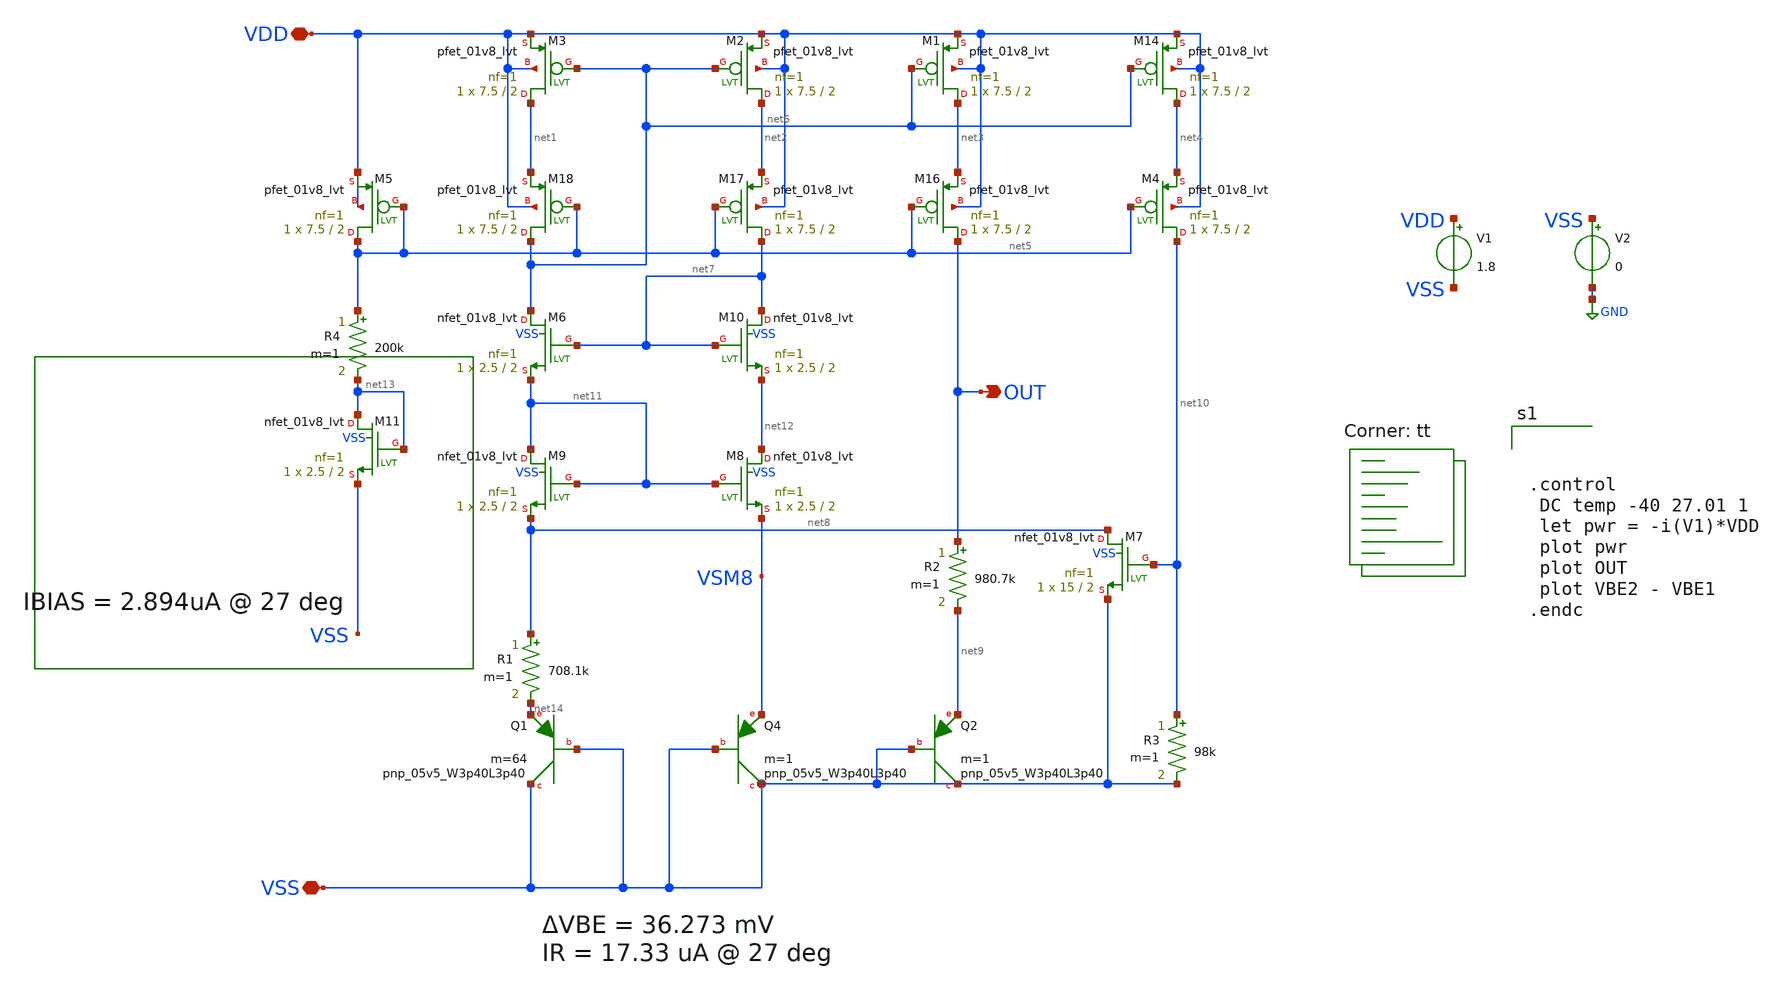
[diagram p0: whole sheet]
** sch_path: bandgap/tb_bgr1/temp-sweep.sch
**.subckt temp-sweep VDD VSS OUT
*.iopin VDD
*.iopin VSS
*.opin OUT
V1 VDD VSS 1.8
V2 VSS GND 0
R1 net8 net14 708.1k m=1
R2 OUT net9 980.7k m=1
R3 net10 VSS 98k m=1
XQ4 VSS VSS VSM8 sky130_fd_pr__pnp_05v5_W3p40L3p40 m=1
XQ1 VSS VSS net14 sky130_fd_pr__pnp_05v5_W3p40L3p40 m=64
XQ2 VSS VSS net9 sky130_fd_pr__pnp_05v5_W3p40L3p40 m=1
XM14 net4 net6 VDD VDD sky130_fd_pr__pfet_01v8_lvt L=2 W=7.5 nf=1 ad='int((nf+1)/2) * W/nf * 0.29' as='int((nf+2)/2) * W/nf * 0.29'
+ pd='2*int((nf+1)/2) * (W/nf + 0.29)' ps='2*int((nf+2)/2) * (W/nf + 0.29)' nrd='0.29 / W' nrs='0.29 / W'
+ sa=0 sb=0 sd=0 mult=1 m=1
XM1 net3 net6 VDD VDD sky130_fd_pr__pfet_01v8_lvt L=2 W=7.5 nf=1 ad='int((nf+1)/2) * W/nf * 0.29' as='int((nf+2)/2) * W/nf * 0.29'
+ pd='2*int((nf+1)/2) * (W/nf + 0.29)' ps='2*int((nf+2)/2) * (W/nf + 0.29)' nrd='0.29 / W' nrs='0.29 / W'
+ sa=0 sb=0 sd=0 mult=1 m=1
XM2 net2 net6 VDD VDD sky130_fd_pr__pfet_01v8_lvt L=2 W=7.5 nf=1 ad='int((nf+1)/2) * W/nf * 0.29' as='int((nf+2)/2) * W/nf * 0.29'
+ pd='2*int((nf+1)/2) * (W/nf + 0.29)' ps='2*int((nf+2)/2) * (W/nf + 0.29)' nrd='0.29 / W' nrs='0.29 / W'
+ sa=0 sb=0 sd=0 mult=1 m=1
XM3 net1 net6 VDD VDD sky130_fd_pr__pfet_01v8_lvt L=2 W=7.5 nf=1 ad='int((nf+1)/2) * W/nf * 0.29' as='int((nf+2)/2) * W/nf * 0.29'
+ pd='2*int((nf+1)/2) * (W/nf + 0.29)' ps='2*int((nf+2)/2) * (W/nf + 0.29)' nrd='0.29 / W' nrs='0.29 / W'
+ sa=0 sb=0 sd=0 mult=1 m=1
XM4 net10 net5 net4 VDD sky130_fd_pr__pfet_01v8_lvt L=2 W=7.5 nf=1 ad='int((nf+1)/2) * W/nf * 0.29' as='int((nf+2)/2) * W/nf * 0.29'
+ pd='2*int((nf+1)/2) * (W/nf + 0.29)' ps='2*int((nf+2)/2) * (W/nf + 0.29)' nrd='0.29 / W' nrs='0.29 / W'
+ sa=0 sb=0 sd=0 mult=1 m=1
XM16 OUT net5 net3 VDD sky130_fd_pr__pfet_01v8_lvt L=2 W=7.5 nf=1 ad='int((nf+1)/2) * W/nf * 0.29' as='int((nf+2)/2) * W/nf * 0.29'
+ pd='2*int((nf+1)/2) * (W/nf + 0.29)' ps='2*int((nf+2)/2) * (W/nf + 0.29)' nrd='0.29 / W' nrs='0.29 / W'
+ sa=0 sb=0 sd=0 mult=1 m=1
XM17 net7 net5 net2 VDD sky130_fd_pr__pfet_01v8_lvt L=2 W=7.5 nf=1 ad='int((nf+1)/2) * W/nf * 0.29' as='int((nf+2)/2) * W/nf * 0.29'
+ pd='2*int((nf+1)/2) * (W/nf + 0.29)' ps='2*int((nf+2)/2) * (W/nf + 0.29)' nrd='0.29 / W' nrs='0.29 / W'
+ sa=0 sb=0 sd=0 mult=1 m=1
XM18 net6 net5 net1 VDD sky130_fd_pr__pfet_01v8_lvt L=2 W=7.5 nf=1 ad='int((nf+1)/2) * W/nf * 0.29' as='int((nf+2)/2) * W/nf * 0.29'
+ pd='2*int((nf+1)/2) * (W/nf + 0.29)' ps='2*int((nf+2)/2) * (W/nf + 0.29)' nrd='0.29 / W' nrs='0.29 / W'
+ sa=0 sb=0 sd=0 mult=1 m=1
XM5 net5 net5 VDD VDD sky130_fd_pr__pfet_01v8_lvt L=2 W=7.5 nf=1 ad='int((nf+1)/2) * W/nf * 0.29' as='int((nf+2)/2) * W/nf * 0.29'
+ pd='2*int((nf+1)/2) * (W/nf + 0.29)' ps='2*int((nf+2)/2) * (W/nf + 0.29)' nrd='0.29 / W' nrs='0.29 / W'
+ sa=0 sb=0 sd=0 mult=1 m=1
XM10 net7 net7 net12 VSS sky130_fd_pr__nfet_01v8_lvt L=2 W=2.5 nf=1 ad='int((nf+1)/2) * W/nf * 0.29'
+ as='int((nf+2)/2) * W/nf * 0.29' pd='2*int((nf+1)/2) * (W/nf + 0.29)' ps='2*int((nf+2)/2) * (W/nf + 0.29)'
+ nrd='0.29 / W' nrs='0.29 / W' sa=0 sb=0 sd=0 mult=1 m=1
XM6 net6 net7 net11 VSS sky130_fd_pr__nfet_01v8_lvt L=2 W=2.5 nf=1 ad='int((nf+1)/2) * W/nf * 0.29' as='int((nf+2)/2) * W/nf * 0.29'
+ pd='2*int((nf+1)/2) * (W/nf + 0.29)' ps='2*int((nf+2)/2) * (W/nf + 0.29)' nrd='0.29 / W' nrs='0.29 / W'
+ sa=0 sb=0 sd=0 mult=1 m=1
XM7 net8 net10 VSS VSS sky130_fd_pr__nfet_01v8_lvt L=2 W=15 nf=1 ad='int((nf+1)/2) * W/nf * 0.29' as='int((nf+2)/2) * W/nf * 0.29'
+ pd='2*int((nf+1)/2) * (W/nf + 0.29)' ps='2*int((nf+2)/2) * (W/nf + 0.29)' nrd='0.29 / W' nrs='0.29 / W'
+ sa=0 sb=0 sd=0 mult=1 m=1
XM8 net12 net11 VSM8 VSS sky130_fd_pr__nfet_01v8_lvt L=2 W=2.5 nf=1 ad='int((nf+1)/2) * W/nf * 0.29'
+ as='int((nf+2)/2) * W/nf * 0.29' pd='2*int((nf+1)/2) * (W/nf + 0.29)' ps='2*int((nf+2)/2) * (W/nf + 0.29)'
+ nrd='0.29 / W' nrs='0.29 / W' sa=0 sb=0 sd=0 mult=1 m=1
XM9 net11 net11 net8 VSS sky130_fd_pr__nfet_01v8_lvt L=2 W=2.5 nf=1 ad='int((nf+1)/2) * W/nf * 0.29'
+ as='int((nf+2)/2) * W/nf * 0.29' pd='2*int((nf+1)/2) * (W/nf + 0.29)' ps='2*int((nf+2)/2) * (W/nf + 0.29)'
+ nrd='0.29 / W' nrs='0.29 / W' sa=0 sb=0 sd=0 mult=1 m=1
R4 net5 net13 200k m=1
XM11 net13 net13 VSS VSS sky130_fd_pr__nfet_01v8_lvt L=2 W=2.5 nf=1 ad='int((nf+1)/2) * W/nf * 0.29'
+ as='int((nf+2)/2) * W/nf * 0.29' pd='2*int((nf+1)/2) * (W/nf + 0.29)' ps='2*int((nf+2)/2) * (W/nf + 0.29)'
+ nrd='0.29 / W' nrs='0.29 / W' sa=0 sb=0 sd=0 mult=1 m=1
**** begin user architecture code
.lib $::SKYWATER_MODELS/sky130.lib.spice tt



.control
 DC temp -40 27.01 1
 let pwr = -i(V1)*VDD
 plot pwr
 plot OUT
 plot VBE2 - VBE1
.endc


**** end user architecture code
**.ends
.GLOBAL GND
.end
